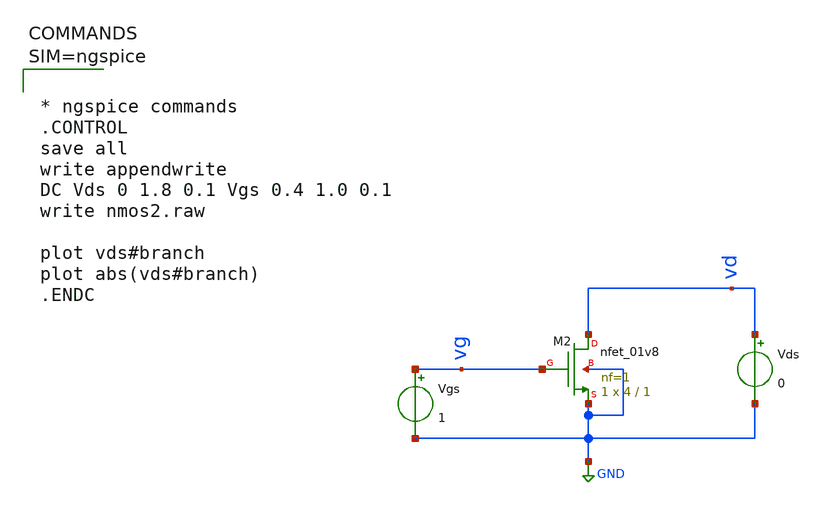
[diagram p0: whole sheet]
** sch_path: work/xschem/nmos2.sch
**.subckt nmos2
XM2 vd vg GND GND sky130_fd_pr__nfet_01v8 L=1 W=4 nf=1 ad='int((1 + 1)/2) * 4 / 1 * 0.29' as='int((1 + 2)/2) * 4 / 1 * 0.29'
+ pd='2*int((1 + 1)/2) * (4 / 1 + 0.29)' ps='2*int((1 + 2)/2) * (4 / 1 + 0.29)' nrd='0.29 / 4 ' nrs='0.29 / 4 '
+ sa=0 sb=0 sd=0 mult=1 m=1
Vgs vg GND 1
Vds vd GND 0
**** begin user architecture code



* ngspice commands
.CONTROL
save all
write appendwrite
DC Vds 0 1.8 0.1 Vgs 0.4 1.0 0.1
write nmos2.raw

plot vds#branch
plot abs(vds#branch)
.ENDC




** opencircuitdesign pdks install
.lib $::SKYWATER_MODELS/sky130.lib.spice tt

**** end user architecture code
**.ends
.GLOBAL GND
.end
